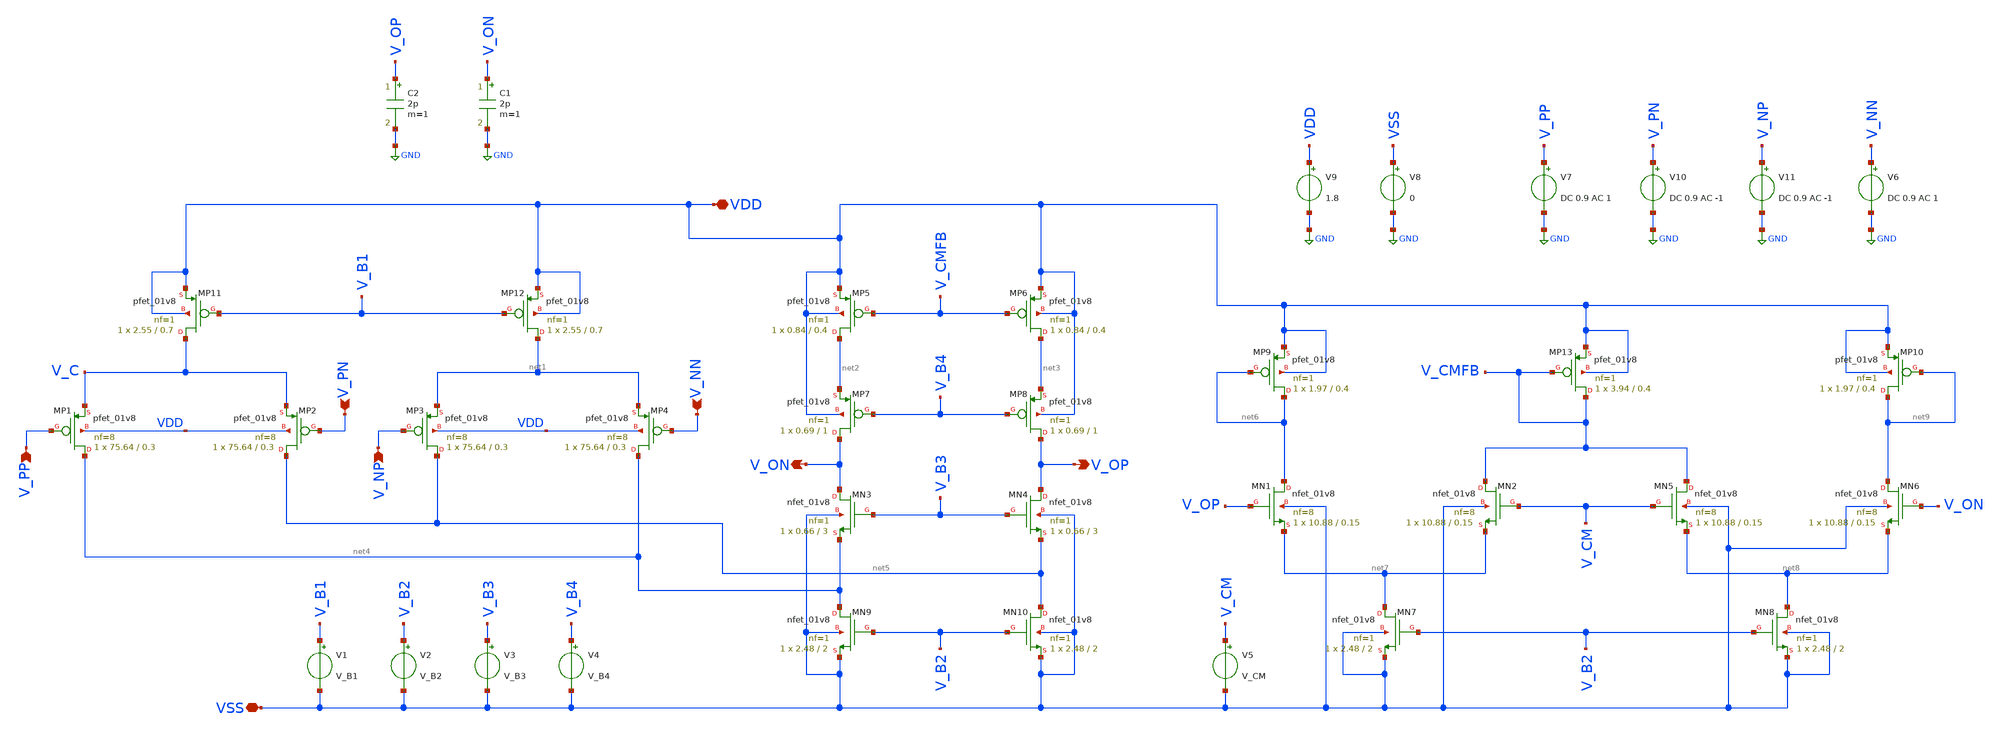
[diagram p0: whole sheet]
** sch_path: SMACD Results/Simulations/Schematics/tb_FDDA_CMFB_v3.sch
**.subckt tb_FDDA_CMFB_v3 V_PP V_PN V_NP V_NN VDD VSS V_OP V_ON
*.ipin V_PP
*.ipin V_PN
*.ipin V_NP
*.ipin V_NN
*.iopin VDD
*.iopin VSS
*.opin V_OP
*.opin V_ON
XMP1 net4 V_PP V_C VDD sky130_fd_pr__pfet_01v8 L=0.3 W=75.64 nf=8 ad='int((8 + 1)/2) * 75.64 / 8 * 0.29'
+ as='int((8 + 2)/2) * 75.64 / 8 * 0.29' pd='2*int((8 + 1)/2) * (75.64 / 8 + 0.29)' ps='2*int((8 + 2)/2) * (75.64 / 8 + 0.29)'
+ nrd='0.29 / 75.64 ' nrs='0.29 / 75.64 ' sa=0 sb=0 sd=0 mult=1 m=1
XMP2 net5 V_PN V_C VDD sky130_fd_pr__pfet_01v8 L=0.3 W=75.64 nf=8 ad='int((8 + 1)/2) * 75.64 / 8 * 0.29'
+ as='int((8 + 2)/2) * 75.64 / 8 * 0.29' pd='2*int((8 + 1)/2) * (75.64 / 8 + 0.29)' ps='2*int((8 + 2)/2) * (75.64 / 8 + 0.29)'
+ nrd='0.29 / 75.64 ' nrs='0.29 / 75.64 ' sa=0 sb=0 sd=0 mult=1 m=1
XMP3 net5 V_NP net1 VDD sky130_fd_pr__pfet_01v8 L=0.3 W=75.64 nf=8 ad='int((8 + 1)/2) * 75.64 / 8 * 0.29'
+ as='int((8 + 2)/2) * 75.64 / 8 * 0.29' pd='2*int((8 + 1)/2) * (75.64 / 8 + 0.29)' ps='2*int((8 + 2)/2) * (75.64 / 8 + 0.29)'
+ nrd='0.29 / 75.64 ' nrs='0.29 / 75.64 ' sa=0 sb=0 sd=0 mult=1 m=1
XMP4 net4 V_NN net1 VDD sky130_fd_pr__pfet_01v8 L=0.3 W=75.64 nf=8 ad='int((8 + 1)/2) * 75.64 / 8 * 0.29'
+ as='int((8 + 2)/2) * 75.64 / 8 * 0.29' pd='2*int((8 + 1)/2) * (75.64 / 8 + 0.29)' ps='2*int((8 + 2)/2) * (75.64 / 8 + 0.29)'
+ nrd='0.29 / 75.64 ' nrs='0.29 / 75.64 ' sa=0 sb=0 sd=0 mult=1 m=1
XMP5 net2 V_CMFB VDD VDD sky130_fd_pr__pfet_01v8 L=0.4 W=0.84 nf=1 ad='int((1 + 1)/2) * 0.84 / 1 * 0.29'
+ as='int((1 + 2)/2) * 0.84 / 1 * 0.29' pd='2*int((1 + 1)/2) * (0.84 / 1 + 0.29)' ps='2*int((1 + 2)/2) * (0.84 / 1 + 0.29)'
+ nrd='0.29 / 0.84 ' nrs='0.29 / 0.84 ' sa=0 sb=0 sd=0 mult=1 m=1
XMP6 net3 V_CMFB VDD VDD sky130_fd_pr__pfet_01v8 L=0.4 W=0.84 nf=1 ad='int((1 + 1)/2) * 0.84 / 1 * 0.29'
+ as='int((1 + 2)/2) * 0.84 / 1 * 0.29' pd='2*int((1 + 1)/2) * (0.84 / 1 + 0.29)' ps='2*int((1 + 2)/2) * (0.84 / 1 + 0.29)'
+ nrd='0.29 / 0.84 ' nrs='0.29 / 0.84 ' sa=0 sb=0 sd=0 mult=1 m=1
XMP7 V_ON V_B4 net2 VDD sky130_fd_pr__pfet_01v8 L=1 W=0.69 nf=1 ad='int((1 + 1)/2) * 0.69 / 1 * 0.29'
+ as='int((1 + 2)/2) * 0.69 / 1 * 0.29' pd='2*int((1 + 1)/2) * (0.69 / 1 + 0.29)' ps='2*int((1 + 2)/2) * (0.69 / 1 + 0.29)'
+ nrd='0.29 / 0.69 ' nrs='0.29 / 0.69 ' sa=0 sb=0 sd=0 mult=1 m=1
XMP8 V_OP V_B4 net3 VDD sky130_fd_pr__pfet_01v8 L=1 W=0.69 nf=1 ad='int((1 + 1)/2) * 0.69 / 1 * 0.29'
+ as='int((1 + 2)/2) * 0.69 / 1 * 0.29' pd='2*int((1 + 1)/2) * (0.69 / 1 + 0.29)' ps='2*int((1 + 2)/2) * (0.69 / 1 + 0.29)'
+ nrd='0.29 / 0.69 ' nrs='0.29 / 0.69 ' sa=0 sb=0 sd=0 mult=1 m=1
XMP11 V_C V_B1 VDD VDD sky130_fd_pr__pfet_01v8 L=0.7 W=2.55 nf=1 ad='int((1 + 1)/2) * 2.55 / 1 * 0.29'
+ as='int((1 + 2)/2) * 2.55 / 1 * 0.29' pd='2*int((1 + 1)/2) * (2.55 / 1 + 0.29)' ps='2*int((1 + 2)/2) * (2.55 / 1 + 0.29)'
+ nrd='0.29 / 2.55 ' nrs='0.29 / 2.55 ' sa=0 sb=0 sd=0 mult=1 m=1
XMP12 net1 V_B1 VDD VDD sky130_fd_pr__pfet_01v8 L=0.7 W=2.55 nf=1 ad='int((1 + 1)/2) * 2.55 / 1 * 0.29'
+ as='int((1 + 2)/2) * 2.55 / 1 * 0.29' pd='2*int((1 + 1)/2) * (2.55 / 1 + 0.29)' ps='2*int((1 + 2)/2) * (2.55 / 1 + 0.29)'
+ nrd='0.29 / 2.55 ' nrs='0.29 / 2.55 ' sa=0 sb=0 sd=0 mult=1 m=1
XMN3 V_ON V_B3 net4 VSS sky130_fd_pr__nfet_01v8 L=3 W=0.66 nf=1 ad='int((1 + 1)/2) * 0.66 / 1 * 0.29'
+ as='int((1 + 2)/2) * 0.66 / 1 * 0.29' pd='2*int((1 + 1)/2) * (0.66 / 1 + 0.29)' ps='2*int((1 + 2)/2) * (0.66 / 1 + 0.29)'
+ nrd='0.29 / 0.66 ' nrs='0.29 / 0.66 ' sa=0 sb=0 sd=0 mult=1 m=1
XMN4 V_OP V_B3 net5 VSS sky130_fd_pr__nfet_01v8 L=3 W=0.66 nf=1 ad='int((1 + 1)/2) * 0.66 / 1 * 0.29'
+ as='int((1 + 2)/2) * 0.66 / 1 * 0.29' pd='2*int((1 + 1)/2) * (0.66 / 1 + 0.29)' ps='2*int((1 + 2)/2) * (0.66 / 1 + 0.29)'
+ nrd='0.29 / 0.66 ' nrs='0.29 / 0.66 ' sa=0 sb=0 sd=0 mult=1 m=1
XMN9 net4 V_B2 VSS VSS sky130_fd_pr__nfet_01v8 L=2 W=2.48 nf=1 ad='int((1 + 1)/2) * 2.48 / 1 * 0.29'
+ as='int((1 + 2)/2) * 2.48 / 1 * 0.29' pd='2*int((1 + 1)/2) * (2.48 / 1 + 0.29)' ps='2*int((1 + 2)/2) * (2.48 / 1 + 0.29)'
+ nrd='0.29 / 2.48 ' nrs='0.29 / 2.48 ' sa=0 sb=0 sd=0 mult=1 m=1
XMN10 net5 V_B2 VSS VSS sky130_fd_pr__nfet_01v8 L=2 W=2.48 nf=1 ad='int((1 + 1)/2) * 2.48 / 1 * 0.29'
+ as='int((1 + 2)/2) * 2.48 / 1 * 0.29' pd='2*int((1 + 1)/2) * (2.48 / 1 + 0.29)' ps='2*int((1 + 2)/2) * (2.48 / 1 + 0.29)'
+ nrd='0.29 / 2.48 ' nrs='0.29 / 2.48 ' sa=0 sb=0 sd=0 mult=1 m=1
V4 V_B4 VSS V_B4
V3 V_B3 VSS V_B3
V2 V_B2 VSS V_B2
V1 V_B1 VSS V_B1
XMN1 net6 V_OP net7 VSS sky130_fd_pr__nfet_01v8 L=0.15 W=10.88 nf=8 ad='int((8 + 1)/2) * 10.88 / 8 * 0.29'
+ as='int((8 + 2)/2) * 10.88 / 8 * 0.29' pd='2*int((8 + 1)/2) * (10.88 / 8 + 0.29)' ps='2*int((8 + 2)/2) * (10.88 / 8 + 0.29)'
+ nrd='0.29 / 10.88 ' nrs='0.29 / 10.88 ' sa=0 sb=0 sd=0 mult=1 m=1
XMN2 V_CMFB V_CM net7 VSS sky130_fd_pr__nfet_01v8 L=0.15 W=10.88 nf=8 ad='int((8 + 1)/2) * 10.88 / 8 * 0.29'
+ as='int((8 + 2)/2) * 10.88 / 8 * 0.29' pd='2*int((8 + 1)/2) * (10.88 / 8 + 0.29)' ps='2*int((8 + 2)/2) * (10.88 / 8 + 0.29)'
+ nrd='0.29 / 10.88 ' nrs='0.29 / 10.88 ' sa=0 sb=0 sd=0 mult=1 m=1
XMN7 net7 V_B2 VSS VSS sky130_fd_pr__nfet_01v8 L=2 W=2.48 nf=1 ad='int((1 + 1)/2) * 2.48 / 1 * 0.29'
+ as='int((1 + 2)/2) * 2.48 / 1 * 0.29' pd='2*int((1 + 1)/2) * (2.48 / 1 + 0.29)' ps='2*int((1 + 2)/2) * (2.48 / 1 + 0.29)'
+ nrd='0.29 / 2.48 ' nrs='0.29 / 2.48 ' sa=0 sb=0 sd=0 mult=1 m=1
XMN6 net9 V_ON net8 VSS sky130_fd_pr__nfet_01v8 L=0.15 W=10.88 nf=8 ad='int((8 + 1)/2) * 10.88 / 8 * 0.29'
+ as='int((8 + 2)/2) * 10.88 / 8 * 0.29' pd='2*int((8 + 1)/2) * (10.88 / 8 + 0.29)' ps='2*int((8 + 2)/2) * (10.88 / 8 + 0.29)'
+ nrd='0.29 / 10.88 ' nrs='0.29 / 10.88 ' sa=0 sb=0 sd=0 mult=1 m=1
XMN5 V_CMFB V_CM net8 VSS sky130_fd_pr__nfet_01v8 L=0.15 W=10.88 nf=8 ad='int((8 + 1)/2) * 10.88 / 8 * 0.29'
+ as='int((8 + 2)/2) * 10.88 / 8 * 0.29' pd='2*int((8 + 1)/2) * (10.88 / 8 + 0.29)' ps='2*int((8 + 2)/2) * (10.88 / 8 + 0.29)'
+ nrd='0.29 / 10.88 ' nrs='0.29 / 10.88 ' sa=0 sb=0 sd=0 mult=1 m=1
XMN8 net8 V_B2 VSS VSS sky130_fd_pr__nfet_01v8 L=2 W=2.48 nf=1 ad='int((1 + 1)/2) * 2.48 / 1 * 0.29'
+ as='int((1 + 2)/2) * 2.48 / 1 * 0.29' pd='2*int((1 + 1)/2) * (2.48 / 1 + 0.29)' ps='2*int((1 + 2)/2) * (2.48 / 1 + 0.29)'
+ nrd='0.29 / 2.48 ' nrs='0.29 / 2.48 ' sa=0 sb=0 sd=0 mult=1 m=1
XMP9 net6 net6 VDD VDD sky130_fd_pr__pfet_01v8 L=0.4 W=1.97 nf=1 ad='int((1 + 1)/2) * 1.97 / 1 * 0.29'
+ as='int((1 + 2)/2) * 1.97 / 1 * 0.29' pd='2*int((1 + 1)/2) * (1.97 / 1 + 0.29)' ps='2*int((1 + 2)/2) * (1.97 / 1 + 0.29)'
+ nrd='0.29 / 1.97 ' nrs='0.29 / 1.97 ' sa=0 sb=0 sd=0 mult=1 m=1
XMP13 V_CMFB V_CMFB VDD VDD sky130_fd_pr__pfet_01v8 L=0.4 W=3.94 nf=1 ad='int((1 + 1)/2) * 3.94 / 1 * 0.29'
+ as='int((1 + 2)/2) * 3.94 / 1 * 0.29' pd='2*int((1 + 1)/2) * (3.94 / 1 + 0.29)' ps='2*int((1 + 2)/2) * (3.94 / 1 + 0.29)'
+ nrd='0.29 / 3.94 ' nrs='0.29 / 3.94 ' sa=0 sb=0 sd=0 mult=1 m=1
XMP10 net9 net9 VDD VDD sky130_fd_pr__pfet_01v8 L=0.4 W=1.97 nf=1 ad='int((1 + 1)/2) * 1.97 / 1 * 0.29'
+ as='int((1 + 2)/2) * 1.97 / 1 * 0.29' pd='2*int((1 + 1)/2) * (1.97 / 1 + 0.29)' ps='2*int((1 + 2)/2) * (1.97 / 1 + 0.29)'
+ nrd='0.29 / 1.97 ' nrs='0.29 / 1.97 ' sa=0 sb=0 sd=0 mult=1 m=1
V5 V_CM VSS V_CM
V10 V_PN GND DC 0.9 AC -1
V7 V_PP GND DC 0.9 AC 1
V8 VSS GND 0
V9 VDD GND 1.8
V6 V_NN GND DC 0.9 AC 1
V11 V_NP GND DC 0.9 AC -1
C1 V_ON GND 2p m=1
C2 V_OP GND 2p m=1
**** begin user architecture code

** opencircuitdesign pdks install
.lib $::SKYWATER_MODELS/sky130.lib.spice tt



.control
  save all
  ac dec 20 0.1 0.1G

  let vout = v(v_op) - v(v_on)
  let vin_dm = (v(v_pp) - v(v_pn)) - (v(v_np) - v(v_nn))

  let gain_dm = vout / vin_dm
  let db_gain_dm = db(gain_dm)
  let deg_phase = 180*cph(v(vout))/pi

  meas ac gain_dm_DC FIND db_gain_dm AT=1

  meas ac gbw_freq WHEN db_gain_dm=0 FALL=1
  let gbw_Mfreq = gbw_freq * 1e-6

  meas ac pm_deg FIND deg_phase AT=gbw_freq
  let pm = 180 + pm_deg

  plot db_gain_dm deg_phase
  print gain_dm_DC
  print gbw_Mfreq
  print pm
  wrdata DM.txt db_gain_dm
.endc




.param temp=25
.option savecurrents
.param V_B1=0.6819
.param V_B2=0.6928
.param V_B3=1.0545
.param V_B4=0.2817
.param V_CM=0.9
.control
  save all
  op
  write tb_FDDA_CMFB_v3.raw
.endc


**** end user architecture code
**.ends
.GLOBAL GND
.end
